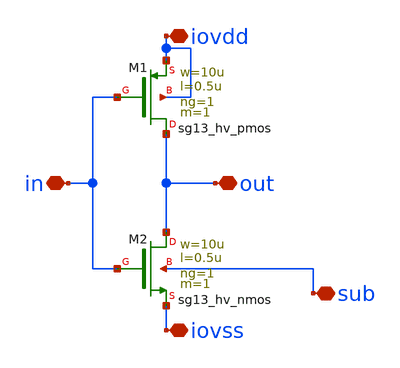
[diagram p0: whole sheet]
** sch_path: ihp-sg13g2/libs.tech/xschem/hm_stdcells/sg13g2_io_inv_hv_noptap.sch
**.subckt sg13g2_io_inv_hv_noptap out iovdd iovss sub in
*.iopin out
*.iopin iovdd
*.iopin iovss
*.iopin sub
*.iopin in
XM1 out in iovdd iovdd sg13_hv_pmos w=10u l=0.5u ng=1 m=1 mm_ok=1
XM2 out in iovss sub sg13_hv_nmos w=10u l=0.5u ng=1 m=1 mm_ok=1
**.ends
.end
